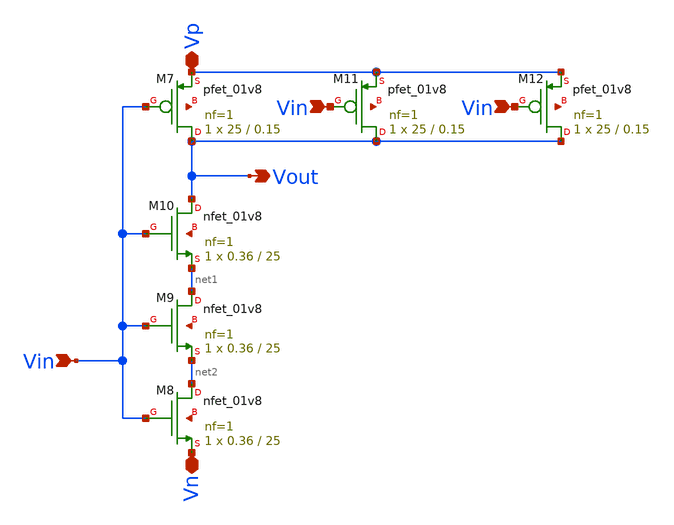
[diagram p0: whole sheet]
** sch_path: xschem/Vth_sch/Inverter-th1.sch
**.subckt Inverter-th1 Vn Vp Vin Vout Vin Vin
*.iopin Vn
*.iopin Vp
*.ipin Vin
*.opin Vout
*.ipin Vin
*.ipin Vin
XM7 Vout Vin Vp net3 sky130_fd_pr__pfet_01v8 L=0.15 W=25 nf=1 ad='int((nf+1)/2) * W/nf * 0.29' as='int((nf+2)/2) * W/nf * 0.29'
+ pd='2*int((nf+1)/2) * (W/nf + 0.29)' ps='2*int((nf+2)/2) * (W/nf + 0.29)' nrd='0.29 / W' nrs='0.29 / W'
+ sa=0 sb=0 sd=0 mult=1 m=1
XM8 net2 Vin Vn net4 sky130_fd_pr__nfet_01v8 L=25 W=0.36 nf=1 ad='int((nf+1)/2) * W/nf * 0.29' as='int((nf+2)/2) * W/nf * 0.29'
+ pd='2*int((nf+1)/2) * (W/nf + 0.29)' ps='2*int((nf+2)/2) * (W/nf + 0.29)' nrd='0.29 / W' nrs='0.29 / W'
+ sa=0 sb=0 sd=0 mult=1 m=1
XM9 net1 Vin net2 net5 sky130_fd_pr__nfet_01v8 L=25 W=0.36 nf=1 ad='int((nf+1)/2) * W/nf * 0.29' as='int((nf+2)/2) * W/nf * 0.29'
+ pd='2*int((nf+1)/2) * (W/nf + 0.29)' ps='2*int((nf+2)/2) * (W/nf + 0.29)' nrd='0.29 / W' nrs='0.29 / W'
+ sa=0 sb=0 sd=0 mult=1 m=1
XM10 Vout Vin net1 net6 sky130_fd_pr__nfet_01v8 L=25 W=0.36 nf=1 ad='int((nf+1)/2) * W/nf * 0.29' as='int((nf+2)/2) * W/nf * 0.29'
+ pd='2*int((nf+1)/2) * (W/nf + 0.29)' ps='2*int((nf+2)/2) * (W/nf + 0.29)' nrd='0.29 / W' nrs='0.29 / W'
+ sa=0 sb=0 sd=0 mult=1 m=1
XM11 Vout Vin Vp net7 sky130_fd_pr__pfet_01v8 L=0.15 W=25 nf=1 ad='int((nf+1)/2) * W/nf * 0.29' as='int((nf+2)/2) * W/nf * 0.29'
+ pd='2*int((nf+1)/2) * (W/nf + 0.29)' ps='2*int((nf+2)/2) * (W/nf + 0.29)' nrd='0.29 / W' nrs='0.29 / W'
+ sa=0 sb=0 sd=0 mult=1 m=1
XM12 Vout Vin Vp net8 sky130_fd_pr__pfet_01v8 L=0.15 W=25 nf=1 ad='int((nf+1)/2) * W/nf * 0.29' as='int((nf+2)/2) * W/nf * 0.29'
+ pd='2*int((nf+1)/2) * (W/nf + 0.29)' ps='2*int((nf+2)/2) * (W/nf + 0.29)' nrd='0.29 / W' nrs='0.29 / W'
+ sa=0 sb=0 sd=0 mult=1 m=1
**.ends
.end
